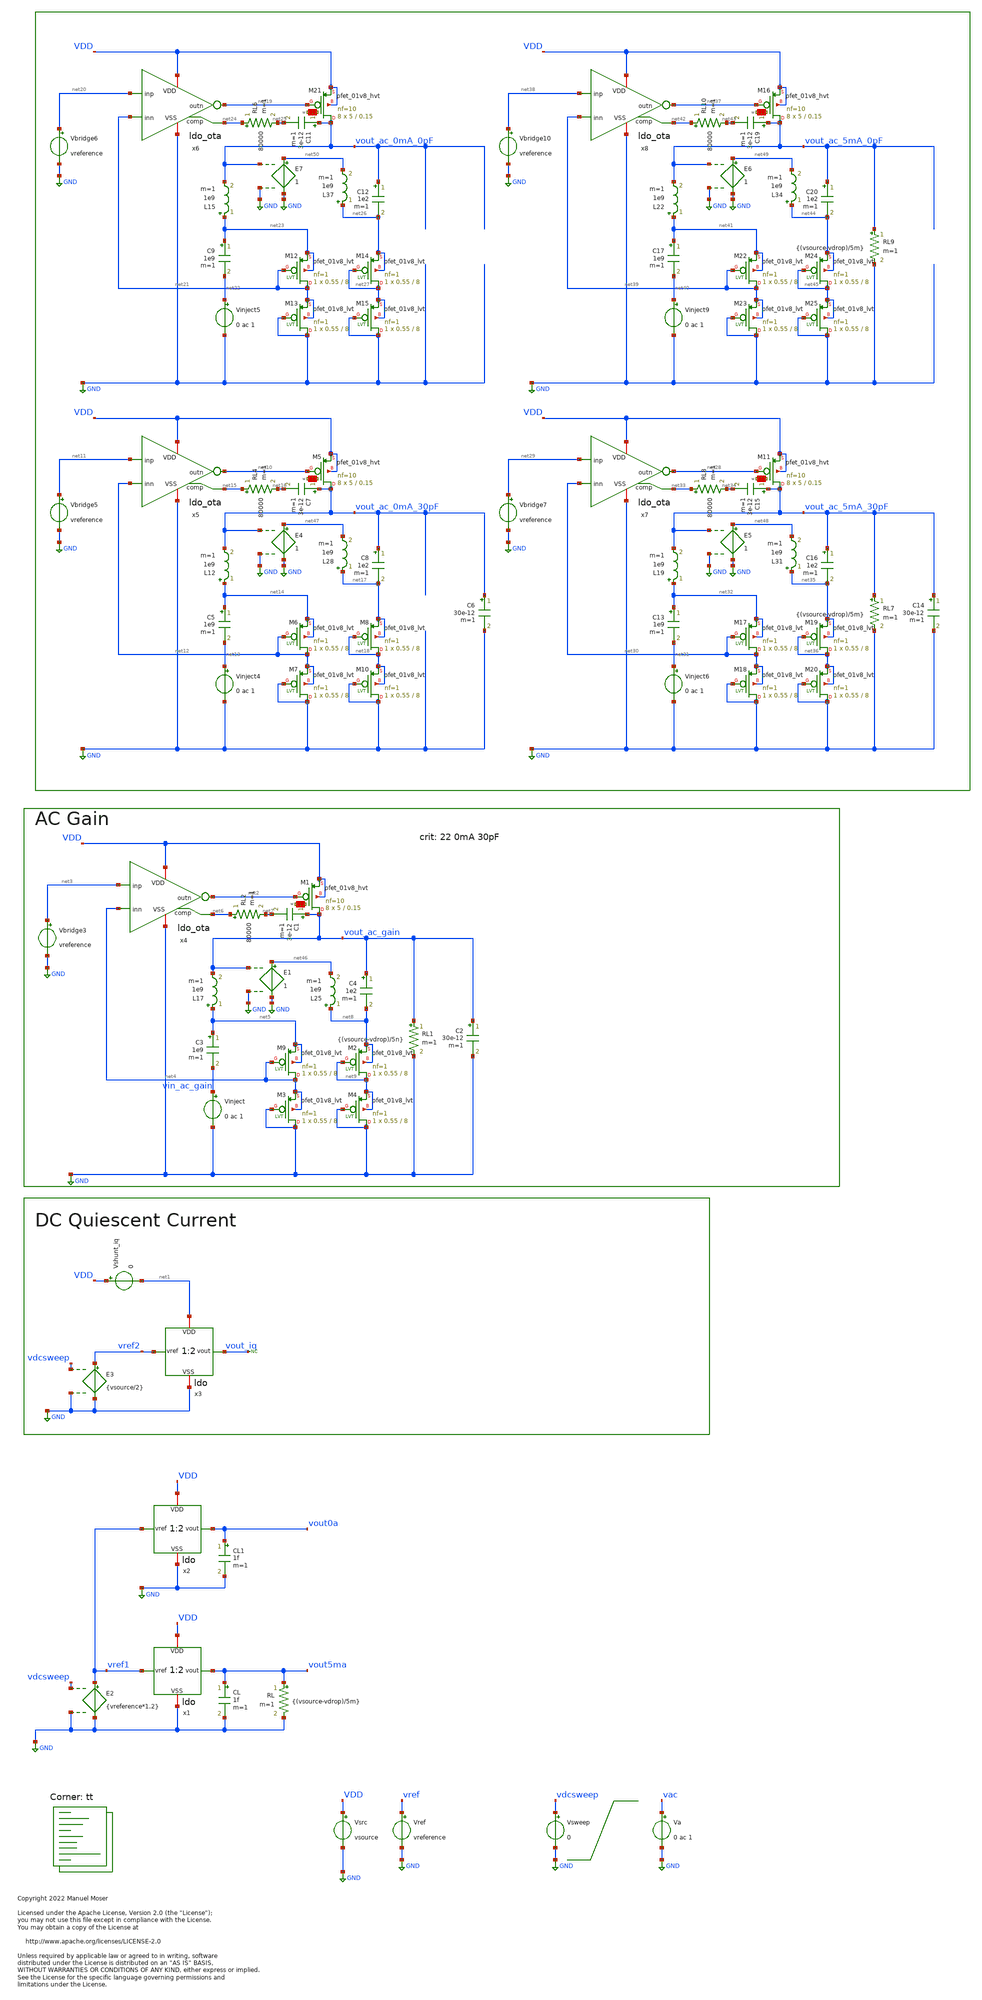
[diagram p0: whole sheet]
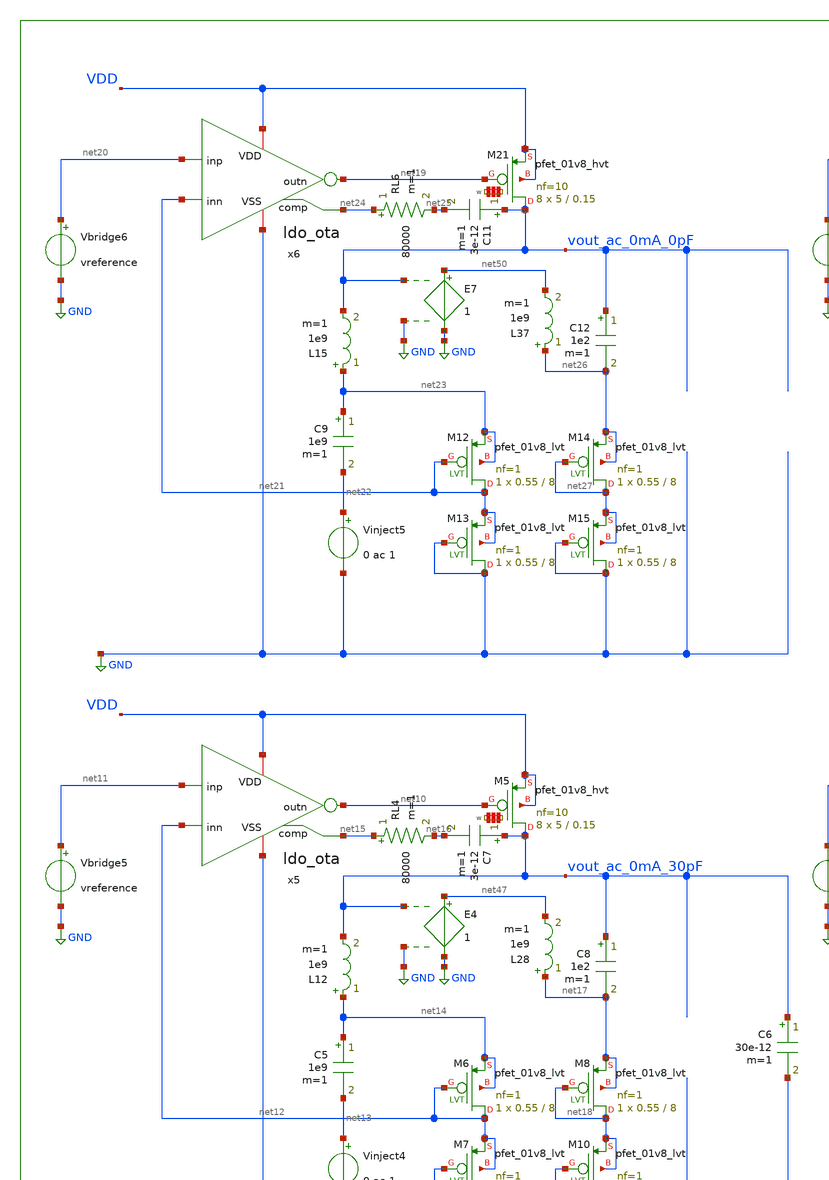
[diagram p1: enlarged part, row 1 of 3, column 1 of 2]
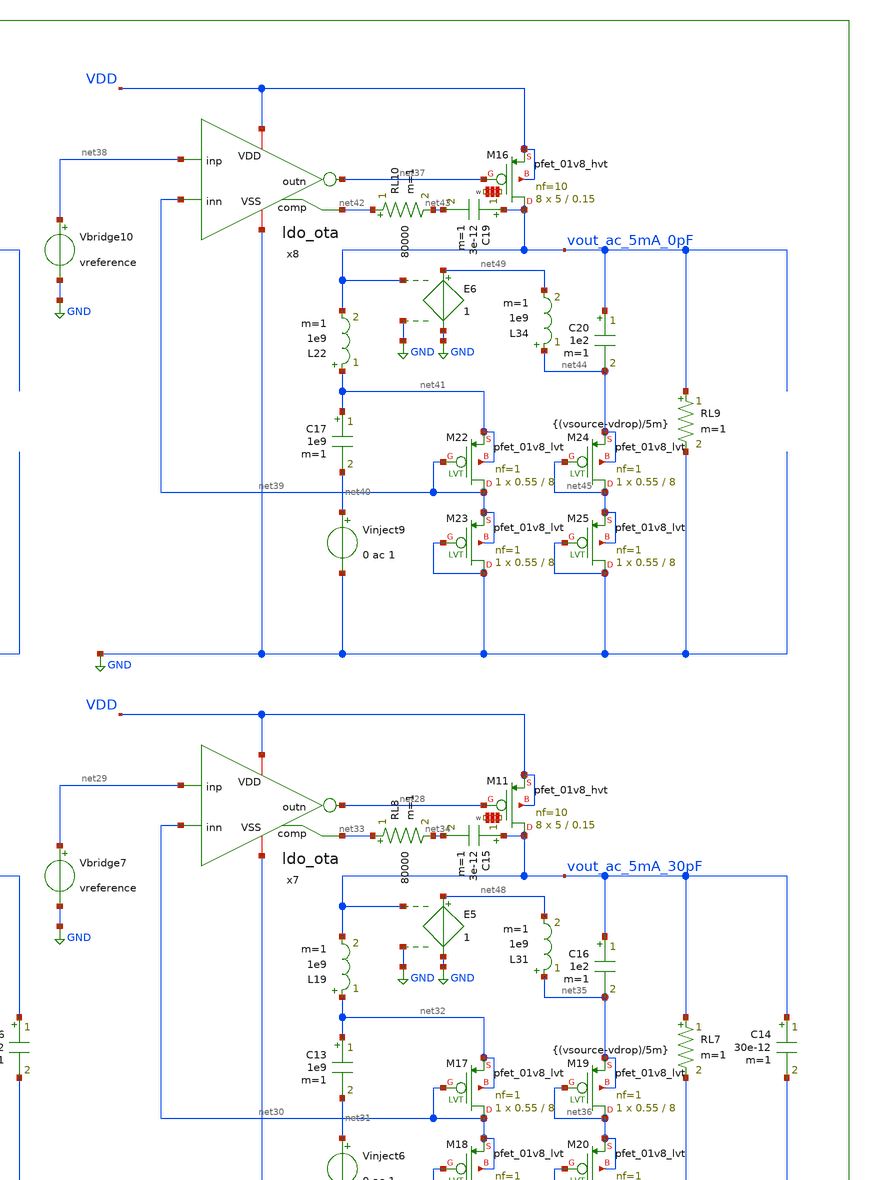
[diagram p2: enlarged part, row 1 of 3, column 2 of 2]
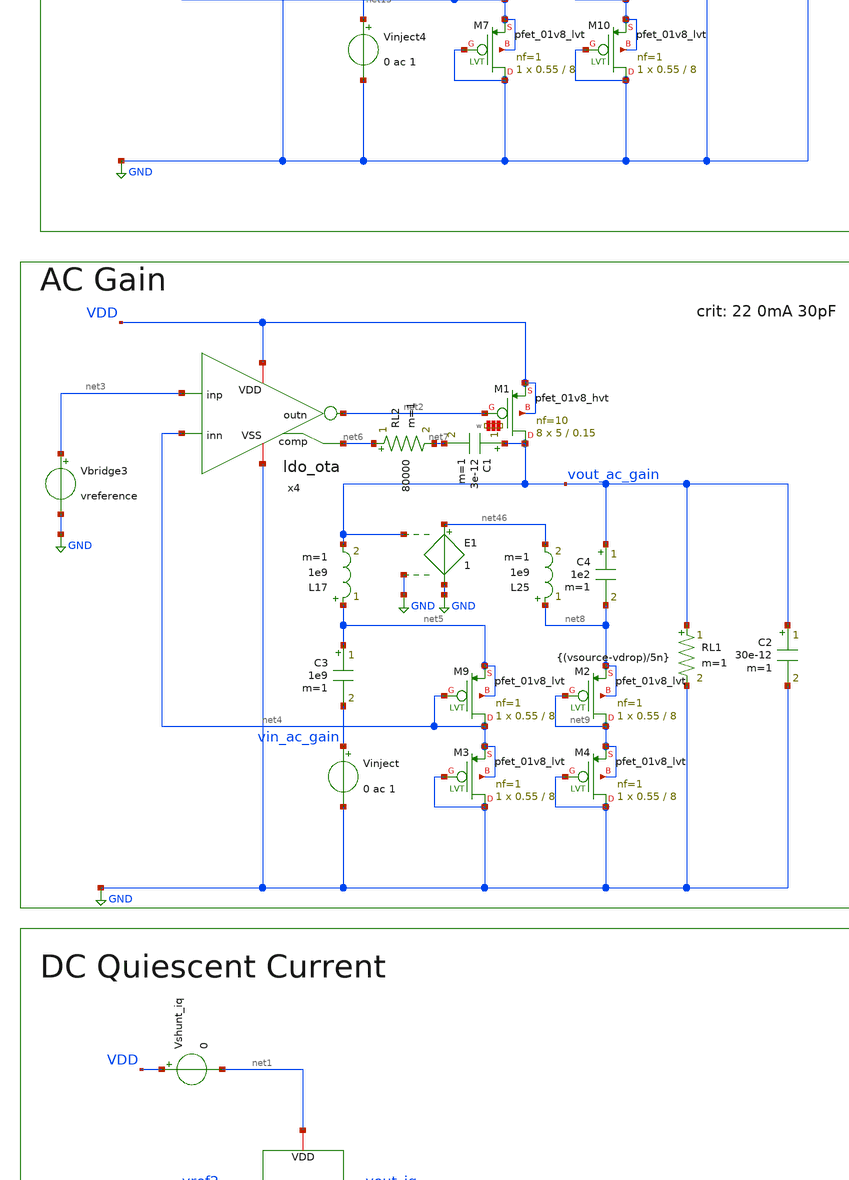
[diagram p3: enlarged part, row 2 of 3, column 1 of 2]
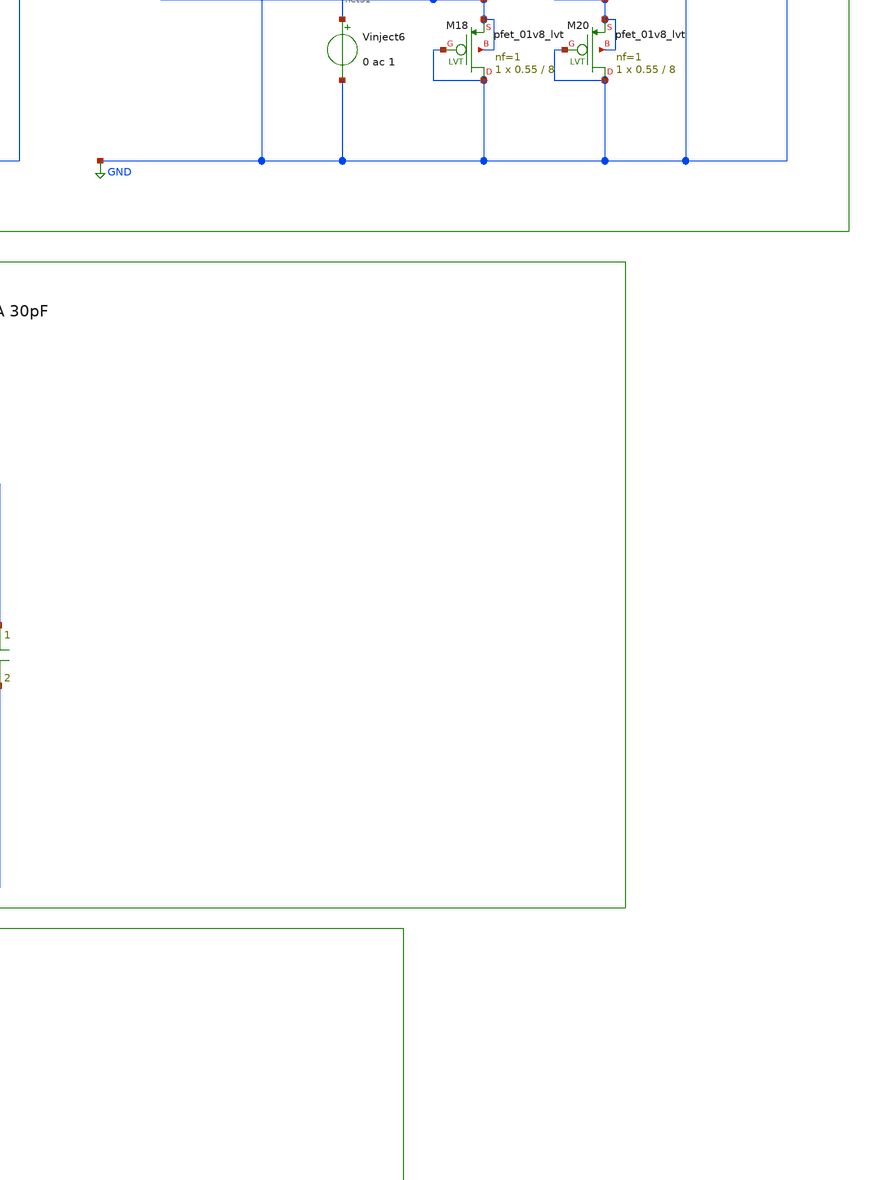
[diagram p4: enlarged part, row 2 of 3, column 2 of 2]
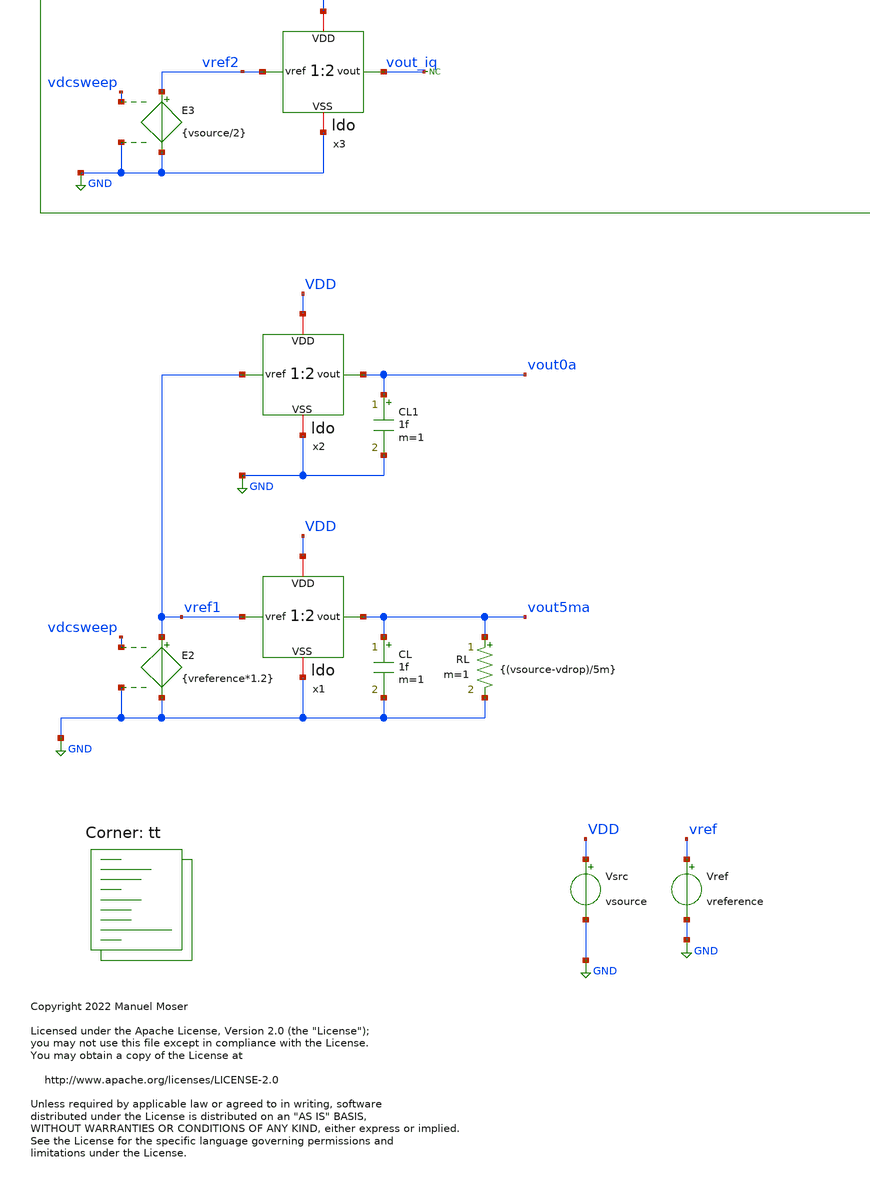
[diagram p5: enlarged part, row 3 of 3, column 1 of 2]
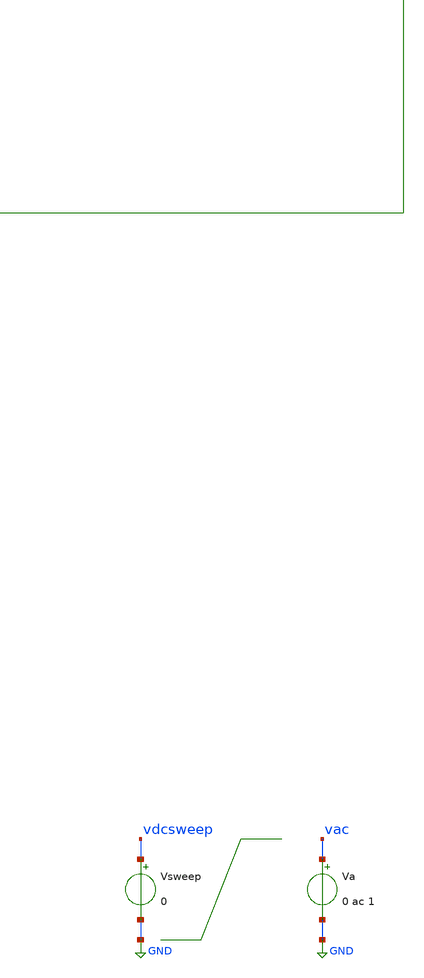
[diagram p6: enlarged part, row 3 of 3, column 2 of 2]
** sch_path: xschem/ldo_tb.sch
* Copyright 2022 Manuel Moser
* Licensed under the Apache License, Version 2.0 (the "License");
**.subckt ldo_tb
Vref vref GND vreference
Vsrc VDD GND vsource
Va vac GND 0 ac 1
CL vout5ma GND 1f m=1
RL vout5ma GND {(vsource-vdrop)/5m} m=1
x1 VDD vref1 vout5ma GND ldo
CL1 vout0a GND 1f m=1
x2 VDD vref1 vout0a GND ldo
Vsweep vdcsweep GND 0
E2 vref1 GND vdcsweep GND {vreference*1.2}
x3 net1 vref2 vout_iq GND ldo
Vshunt_iq VDD net1 0
E3 vref2 GND vdcsweep GND {vsource/2}
* noconn vout_iq
x4 VDD net3 net2 net4 GND net6 ldo_ota
L17 net5 vout_ac_gain 1e9 m=1
C3 net5 vin_ac_gain 1e9 m=1
Vinject vin_ac_gain GND 0 ac 1
Vbridge3 net3 GND vreference
RL1 vout_ac_gain GND {(vsource-vdrop)/5n} m=1
C2 vout_ac_gain GND 30e-12 m=1
C1 vout_ac_gain net7 3e-12 m=1
RL2 net6 net7 80000 m=1
XM9 net4 net4 net5 net5 sky130_fd_pr__pfet_01v8_lvt L=8 W=0.55 nf=1 ad='int((nf+1)/2) * W/nf * 0.29'
+ as='int((nf+2)/2) * W/nf * 0.29' pd='2*int((nf+1)/2) * (W/nf + 0.29)' ps='2*int((nf+2)/2) * (W/nf + 0.29)'
+ nrd='0.29 / W' nrs='0.29 / W' sa=0 sb=0 sd=0 mult=1 m=1
XM3 GND GND net4 net4 sky130_fd_pr__pfet_01v8_lvt L=8 W=0.55 nf=1 ad='int((nf+1)/2) * W/nf * 0.29' as='int((nf+2)/2) * W/nf * 0.29'
+ pd='2*int((nf+1)/2) * (W/nf + 0.29)' ps='2*int((nf+2)/2) * (W/nf + 0.29)' nrd='0.29 / W' nrs='0.29 / W'
+ sa=0 sb=0 sd=0 mult=1 m=1
XM2 net9 net9 net8 net8 sky130_fd_pr__pfet_01v8_lvt L=8 W=0.55 nf=1 ad='int((nf+1)/2) * W/nf * 0.29'
+ as='int((nf+2)/2) * W/nf * 0.29' pd='2*int((nf+1)/2) * (W/nf + 0.29)' ps='2*int((nf+2)/2) * (W/nf + 0.29)'
+ nrd='0.29 / W' nrs='0.29 / W' sa=0 sb=0 sd=0 mult=1 m=1
XM4 GND GND net9 net9 sky130_fd_pr__pfet_01v8_lvt L=8 W=0.55 nf=1 ad='int((nf+1)/2) * W/nf * 0.29' as='int((nf+2)/2) * W/nf * 0.29'
+ pd='2*int((nf+1)/2) * (W/nf + 0.29)' ps='2*int((nf+2)/2) * (W/nf + 0.29)' nrd='0.29 / W' nrs='0.29 / W'
+ sa=0 sb=0 sd=0 mult=1 m=1
C4 vout_ac_gain net8 1e2 m=1
x5 VDD net11 net10 net12 GND net15 ldo_ota
L12 net14 vout_ac_0mA_30pF 1e9 m=1
C5 net14 net13 1e9 m=1
Vinject4 net13 GND 0 ac 1
Vbridge5 net11 GND vreference
C6 vout_ac_0mA_30pF GND 30e-12 m=1
C7 vout_ac_0mA_30pF net16 3e-12 m=1
RL4 net15 net16 80000 m=1
XM6 net12 net12 net14 net14 sky130_fd_pr__pfet_01v8_lvt L=8 W=0.55 nf=1 ad='int((nf+1)/2) * W/nf * 0.29'
+ as='int((nf+2)/2) * W/nf * 0.29' pd='2*int((nf+1)/2) * (W/nf + 0.29)' ps='2*int((nf+2)/2) * (W/nf + 0.29)'
+ nrd='0.29 / W' nrs='0.29 / W' sa=0 sb=0 sd=0 mult=1 m=1
XM7 GND GND net12 net12 sky130_fd_pr__pfet_01v8_lvt L=8 W=0.55 nf=1 ad='int((nf+1)/2) * W/nf * 0.29'
+ as='int((nf+2)/2) * W/nf * 0.29' pd='2*int((nf+1)/2) * (W/nf + 0.29)' ps='2*int((nf+2)/2) * (W/nf + 0.29)'
+ nrd='0.29 / W' nrs='0.29 / W' sa=0 sb=0 sd=0 mult=1 m=1
XM8 net18 net18 net17 net17 sky130_fd_pr__pfet_01v8_lvt L=8 W=0.55 nf=1 ad='int((nf+1)/2) * W/nf * 0.29'
+ as='int((nf+2)/2) * W/nf * 0.29' pd='2*int((nf+1)/2) * (W/nf + 0.29)' ps='2*int((nf+2)/2) * (W/nf + 0.29)'
+ nrd='0.29 / W' nrs='0.29 / W' sa=0 sb=0 sd=0 mult=1 m=1
XM10 GND GND net18 net18 sky130_fd_pr__pfet_01v8_lvt L=8 W=0.55 nf=1 ad='int((nf+1)/2) * W/nf * 0.29'
+ as='int((nf+2)/2) * W/nf * 0.29' pd='2*int((nf+1)/2) * (W/nf + 0.29)' ps='2*int((nf+2)/2) * (W/nf + 0.29)'
+ nrd='0.29 / W' nrs='0.29 / W' sa=0 sb=0 sd=0 mult=1 m=1
C8 vout_ac_0mA_30pF net17 1e2 m=1
x6 VDD net20 net19 net21 GND net24 ldo_ota
L15 net23 vout_ac_0mA_0pF 1e9 m=1
C9 net23 net22 1e9 m=1
Vinject5 net22 GND 0 ac 1
Vbridge6 net20 GND vreference
C11 vout_ac_0mA_0pF net25 3e-12 m=1
RL6 net24 net25 80000 m=1
XM12 net21 net21 net23 net23 sky130_fd_pr__pfet_01v8_lvt L=8 W=0.55 nf=1 ad='int((nf+1)/2) * W/nf * 0.29'
+ as='int((nf+2)/2) * W/nf * 0.29' pd='2*int((nf+1)/2) * (W/nf + 0.29)' ps='2*int((nf+2)/2) * (W/nf + 0.29)'
+ nrd='0.29 / W' nrs='0.29 / W' sa=0 sb=0 sd=0 mult=1 m=1
XM13 GND GND net21 net21 sky130_fd_pr__pfet_01v8_lvt L=8 W=0.55 nf=1 ad='int((nf+1)/2) * W/nf * 0.29'
+ as='int((nf+2)/2) * W/nf * 0.29' pd='2*int((nf+1)/2) * (W/nf + 0.29)' ps='2*int((nf+2)/2) * (W/nf + 0.29)'
+ nrd='0.29 / W' nrs='0.29 / W' sa=0 sb=0 sd=0 mult=1 m=1
XM14 net27 net27 net26 net26 sky130_fd_pr__pfet_01v8_lvt L=8 W=0.55 nf=1 ad='int((nf+1)/2) * W/nf * 0.29'
+ as='int((nf+2)/2) * W/nf * 0.29' pd='2*int((nf+1)/2) * (W/nf + 0.29)' ps='2*int((nf+2)/2) * (W/nf + 0.29)'
+ nrd='0.29 / W' nrs='0.29 / W' sa=0 sb=0 sd=0 mult=1 m=1
XM15 GND GND net27 net27 sky130_fd_pr__pfet_01v8_lvt L=8 W=0.55 nf=1 ad='int((nf+1)/2) * W/nf * 0.29'
+ as='int((nf+2)/2) * W/nf * 0.29' pd='2*int((nf+1)/2) * (W/nf + 0.29)' ps='2*int((nf+2)/2) * (W/nf + 0.29)'
+ nrd='0.29 / W' nrs='0.29 / W' sa=0 sb=0 sd=0 mult=1 m=1
C12 vout_ac_0mA_0pF net26 1e2 m=1
x7 VDD net29 net28 net30 GND net33 ldo_ota
L19 net32 vout_ac_5mA_30pF 1e9 m=1
C13 net32 net31 1e9 m=1
Vinject6 net31 GND 0 ac 1
Vbridge7 net29 GND vreference
RL7 vout_ac_5mA_30pF GND {(vsource-vdrop)/5m} m=1
C14 vout_ac_5mA_30pF GND 30e-12 m=1
C15 vout_ac_5mA_30pF net34 3e-12 m=1
RL8 net33 net34 80000 m=1
XM17 net30 net30 net32 net32 sky130_fd_pr__pfet_01v8_lvt L=8 W=0.55 nf=1 ad='int((nf+1)/2) * W/nf * 0.29'
+ as='int((nf+2)/2) * W/nf * 0.29' pd='2*int((nf+1)/2) * (W/nf + 0.29)' ps='2*int((nf+2)/2) * (W/nf + 0.29)'
+ nrd='0.29 / W' nrs='0.29 / W' sa=0 sb=0 sd=0 mult=1 m=1
XM18 GND GND net30 net30 sky130_fd_pr__pfet_01v8_lvt L=8 W=0.55 nf=1 ad='int((nf+1)/2) * W/nf * 0.29'
+ as='int((nf+2)/2) * W/nf * 0.29' pd='2*int((nf+1)/2) * (W/nf + 0.29)' ps='2*int((nf+2)/2) * (W/nf + 0.29)'
+ nrd='0.29 / W' nrs='0.29 / W' sa=0 sb=0 sd=0 mult=1 m=1
XM19 net36 net36 net35 net35 sky130_fd_pr__pfet_01v8_lvt L=8 W=0.55 nf=1 ad='int((nf+1)/2) * W/nf * 0.29'
+ as='int((nf+2)/2) * W/nf * 0.29' pd='2*int((nf+1)/2) * (W/nf + 0.29)' ps='2*int((nf+2)/2) * (W/nf + 0.29)'
+ nrd='0.29 / W' nrs='0.29 / W' sa=0 sb=0 sd=0 mult=1 m=1
XM20 GND GND net36 net36 sky130_fd_pr__pfet_01v8_lvt L=8 W=0.55 nf=1 ad='int((nf+1)/2) * W/nf * 0.29'
+ as='int((nf+2)/2) * W/nf * 0.29' pd='2*int((nf+1)/2) * (W/nf + 0.29)' ps='2*int((nf+2)/2) * (W/nf + 0.29)'
+ nrd='0.29 / W' nrs='0.29 / W' sa=0 sb=0 sd=0 mult=1 m=1
C16 vout_ac_5mA_30pF net35 1e2 m=1
x8 VDD net38 net37 net39 GND net42 ldo_ota
L22 net41 vout_ac_5mA_0pF 1e9 m=1
C17 net41 net40 1e9 m=1
Vinject9 net40 GND 0 ac 1
Vbridge10 net38 GND vreference
RL9 vout_ac_5mA_0pF GND {(vsource-vdrop)/5m} m=1
C19 vout_ac_5mA_0pF net43 3e-12 m=1
RL10 net42 net43 80000 m=1
XM22 net39 net39 net41 net41 sky130_fd_pr__pfet_01v8_lvt L=8 W=0.55 nf=1 ad='int((nf+1)/2) * W/nf * 0.29'
+ as='int((nf+2)/2) * W/nf * 0.29' pd='2*int((nf+1)/2) * (W/nf + 0.29)' ps='2*int((nf+2)/2) * (W/nf + 0.29)'
+ nrd='0.29 / W' nrs='0.29 / W' sa=0 sb=0 sd=0 mult=1 m=1
XM23 GND GND net39 net39 sky130_fd_pr__pfet_01v8_lvt L=8 W=0.55 nf=1 ad='int((nf+1)/2) * W/nf * 0.29'
+ as='int((nf+2)/2) * W/nf * 0.29' pd='2*int((nf+1)/2) * (W/nf + 0.29)' ps='2*int((nf+2)/2) * (W/nf + 0.29)'
+ nrd='0.29 / W' nrs='0.29 / W' sa=0 sb=0 sd=0 mult=1 m=1
XM24 net45 net45 net44 net44 sky130_fd_pr__pfet_01v8_lvt L=8 W=0.55 nf=1 ad='int((nf+1)/2) * W/nf * 0.29'
+ as='int((nf+2)/2) * W/nf * 0.29' pd='2*int((nf+1)/2) * (W/nf + 0.29)' ps='2*int((nf+2)/2) * (W/nf + 0.29)'
+ nrd='0.29 / W' nrs='0.29 / W' sa=0 sb=0 sd=0 mult=1 m=1
XM25 GND GND net45 net45 sky130_fd_pr__pfet_01v8_lvt L=8 W=0.55 nf=1 ad='int((nf+1)/2) * W/nf * 0.29'
+ as='int((nf+2)/2) * W/nf * 0.29' pd='2*int((nf+1)/2) * (W/nf + 0.29)' ps='2*int((nf+2)/2) * (W/nf + 0.29)'
+ nrd='0.29 / W' nrs='0.29 / W' sa=0 sb=0 sd=0 mult=1 m=1
C20 vout_ac_5mA_0pF net44 1e2 m=1
L25 net8 net46 1e9 m=1
E1 net46 GND vout_ac_gain GND 1
L28 net17 net47 1e9 m=1
E4 net47 GND vout_ac_0mA_30pF GND 1
L31 net35 net48 1e9 m=1
E5 net48 GND vout_ac_5mA_30pF GND 1
L34 net44 net49 1e9 m=1
E6 net49 GND vout_ac_5mA_0pF GND 1
L37 net26 net50 1e9 m=1
E7 net50 GND vout_ac_0mA_0pF GND 1
XM1 vout_ac_gain net2 VDD VDD sky130_fd_pr__pfet_01v8_hvt L=0.15 W='5 * 10 ' nf=10 ad='int((nf+1)/2) * W / nf * 0.29'
+ as='int((nf+2)/2) * W / nf * 0.29' pd='2*int((nf+1)/2) * (W / nf + 0.29)' ps='2*int((nf+2)/2) * (W / nf + 0.29)'
+ nrd='0.29 / W ' nrs='0.29 / W ' sa=0 sb=0 sd=0 mult=8 m=8
XM5 vout_ac_0mA_30pF net10 VDD VDD sky130_fd_pr__pfet_01v8_hvt L=0.15 W='5 * 10 ' nf=10 ad='int((nf+1)/2) * W / nf * 0.29'
+ as='int((nf+2)/2) * W / nf * 0.29' pd='2*int((nf+1)/2) * (W / nf + 0.29)' ps='2*int((nf+2)/2) * (W / nf + 0.29)'
+ nrd='0.29 / W ' nrs='0.29 / W ' sa=0 sb=0 sd=0 mult=8 m=8
XM11 vout_ac_5mA_30pF net28 VDD VDD sky130_fd_pr__pfet_01v8_hvt L=0.15 W='5 * 10 ' nf=10 ad='int((nf+1)/2) * W / nf * 0.29'
+ as='int((nf+2)/2) * W / nf * 0.29' pd='2*int((nf+1)/2) * (W / nf + 0.29)' ps='2*int((nf+2)/2) * (W / nf + 0.29)'
+ nrd='0.29 / W ' nrs='0.29 / W ' sa=0 sb=0 sd=0 mult=8 m=8
XM16 vout_ac_5mA_0pF net37 VDD VDD sky130_fd_pr__pfet_01v8_hvt L=0.15 W='5 * 10 ' nf=10 ad='int((nf+1)/2) * W / nf * 0.29'
+ as='int((nf+2)/2) * W / nf * 0.29' pd='2*int((nf+1)/2) * (W / nf + 0.29)' ps='2*int((nf+2)/2) * (W / nf + 0.29)'
+ nrd='0.29 / W ' nrs='0.29 / W ' sa=0 sb=0 sd=0 mult=8 m=8
XM21 vout_ac_0mA_0pF net19 VDD VDD sky130_fd_pr__pfet_01v8_hvt L=0.15 W='5 * 10 ' nf=10 ad='int((nf+1)/2) * W / nf * 0.29'
+ as='int((nf+2)/2) * W / nf * 0.29' pd='2*int((nf+1)/2) * (W / nf + 0.29)' ps='2*int((nf+2)/2) * (W / nf + 0.29)'
+ nrd='0.29 / W ' nrs='0.29 / W ' sa=0 sb=0 sd=0 mult=8 m=8
**** begin user architecture code



.temp 27
*.option gmin = 1e-16
.option RSHUNT=1E15
.option method = gear

.param vsource = 1.80
.param vdrop = 0.20
.param vreference = {(vsource-vdrop)/2}

.save all
.options savecurrents

.control
set num_threads = 12
write results_ldo.raw
set appendwrite

repeat 1
reset

dc vsweep 0 1 0.01 temp -30 60 90
*dc vsweep 0 1 0.01
write results_ldo.raw   vref1 vout5ma vout0a x1.vota x1.vfb
+ @m.x1.xm9.msky130_fd_pr__pfet_01v8_lvt[id]  vref2 i(vshunt_iq) vout_ac_gain

ac dec 10 1 10meg
write results_ldo.raw vout_ac_0mA_0pF vout_ac_0mA_30pF vout_ac_5mA_0pF vout_ac_5mA_30pF

*pz vinject gnd vout_ac_gain gnd vol pz


end

.endc




.lib $::SKYWATER_MODELS/sky130.lib.spice tt
**** end user architecture code
**.ends
.GLOBAL GND
.end
